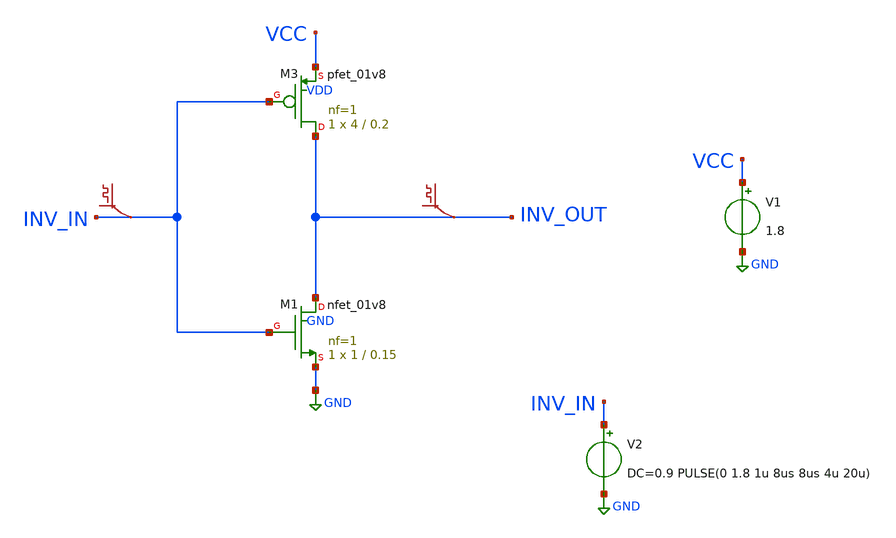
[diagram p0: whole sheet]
** sch_path: xschem/testbench/inverter_tb.sch
**.subckt inverter_tb
XM3 INV_OUT INV_IN VCC VDD sky130_fd_pr__pfet_01v8 L=0.2 W=4 nf=1 ad='int((nf+1)/2) * W/nf * 0.29' as='int((nf+2)/2) * W/nf * 0.29'
+ pd='2*int((nf+1)/2) * (W/nf + 0.29)' ps='2*int((nf+2)/2) * (W/nf + 0.29)' nrd='0.29 / W' nrs='0.29 / W'
+ sa=0 sb=0 sd=0 mult=1 m=1
XM1 INV_OUT INV_IN GND GND sky130_fd_pr__nfet_01v8 L=0.15 W=1 nf=1 ad='int((nf+1)/2) * W/nf * 0.29' as='int((nf+2)/2) * W/nf * 0.29'
+ pd='2*int((nf+1)/2) * (W/nf + 0.29)' ps='2*int((nf+2)/2) * (W/nf + 0.29)' nrd='0.29 / W' nrs='0.29 / W'
+ sa=0 sb=0 sd=0 mult=1 m=1
.save v(inv_out)
.save v(inv_in)
V1 VCC GND 1.8
V2 INV_IN GND DC=0.9 PULSE(0 1.8 1u 8us 8us 4u 20u)
**** begin user architecture code

** opencircuitdesign pdks install
.lib $::SKYWATER_MODELS/sky130.lib.spice tt


**** end user architecture code
**.ends
.GLOBAL GND
**** begin user architecture code


.control
*dc v2 0 1.8 0.05
*plot v(test)
tran 0.1u 40u
*dc v2 0 1.8 0.05
plot v(INV_IN) v(INV_OUT)
write adc_testbench.raw
options filetype=ascii
write adc_testbench.out
.endc


**** end user architecture code
.end
